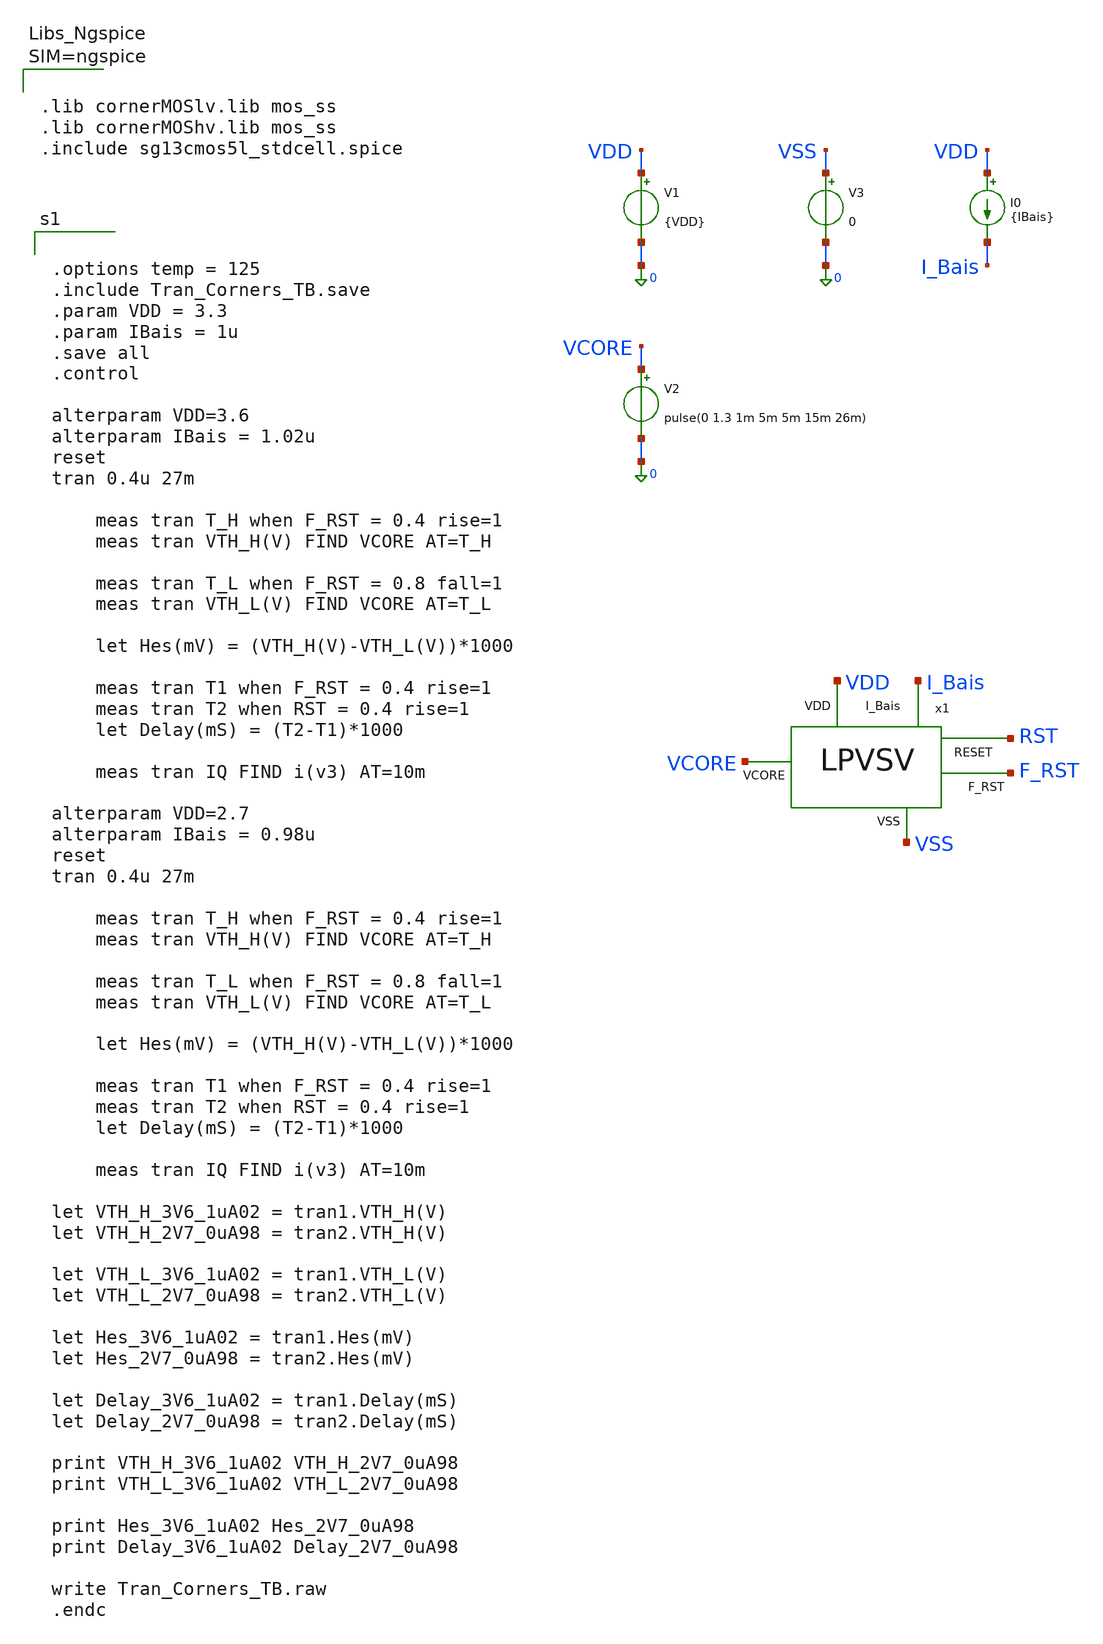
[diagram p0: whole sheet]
** sch_path: Simulation/Tran_Analysis/Tran_Corners_TB.sch
**.subckt Tran_Corners_TB
x1 VDD VCORE I_Bais RST F_RST VSS LPVSV
I0 VDD I_Bais {IBais}
V1 VDD 0 {VDD}
V2 VCORE 0 pulse(0 1.3 1m 5m 5m 15m 26m)
V3 VSS 0 0
**** begin user architecture code



.lib cornerMOSlv.lib mos_ss
.lib cornerMOShv.lib mos_ss
.include sg13cmos5l_stdcell.spice





.options temp = 125
.include Tran_Corners_TB.save
.param VDD = 3.3
.param IBais = 1u
.save all
.control

alterparam VDD=3.6
alterparam IBais = 1.02u
reset
tran 0.4u 27m

	meas tran T_H when F_RST = 0.4 rise=1
	meas tran VTH_H(V) FIND VCORE AT=T_H

	meas tran T_L when F_RST = 0.8 fall=1
	meas tran VTH_L(V) FIND VCORE AT=T_L

	let Hes(mV) = (VTH_H(V)-VTH_L(V))*1000

	meas tran T1 when F_RST = 0.4 rise=1
	meas tran T2 when RST = 0.4 rise=1
	let Delay(mS) = (T2-T1)*1000

	meas tran IQ FIND i(v3) AT=10m

alterparam VDD=2.7
alterparam IBais = 0.98u
reset
tran 0.4u 27m

	meas tran T_H when F_RST = 0.4 rise=1
	meas tran VTH_H(V) FIND VCORE AT=T_H

	meas tran T_L when F_RST = 0.8 fall=1
	meas tran VTH_L(V) FIND VCORE AT=T_L

	let Hes(mV) = (VTH_H(V)-VTH_L(V))*1000

	meas tran T1 when F_RST = 0.4 rise=1
	meas tran T2 when RST = 0.4 rise=1
	let Delay(mS) = (T2-T1)*1000

	meas tran IQ FIND i(v3) AT=10m

let VTH_H_3V6_1uA02 = tran1.VTH_H(V)
let VTH_H_2V7_0uA98 = tran2.VTH_H(V)

let VTH_L_3V6_1uA02 = tran1.VTH_L(V)
let VTH_L_2V7_0uA98 = tran2.VTH_L(V)

let Hes_3V6_1uA02 = tran1.Hes(mV)
let Hes_2V7_0uA98 = tran2.Hes(mV)

let Delay_3V6_1uA02 = tran1.Delay(mS)
let Delay_2V7_0uA98 = tran2.Delay(mS)

print VTH_H_3V6_1uA02 VTH_H_2V7_0uA98
print VTH_L_3V6_1uA02 VTH_L_2V7_0uA98

print Hes_3V6_1uA02 Hes_2V7_0uA98
print Delay_3V6_1uA02 Delay_2V7_0uA98

write Tran_Corners_TB.raw
.endc


**** end user architecture code
**.ends
.end
